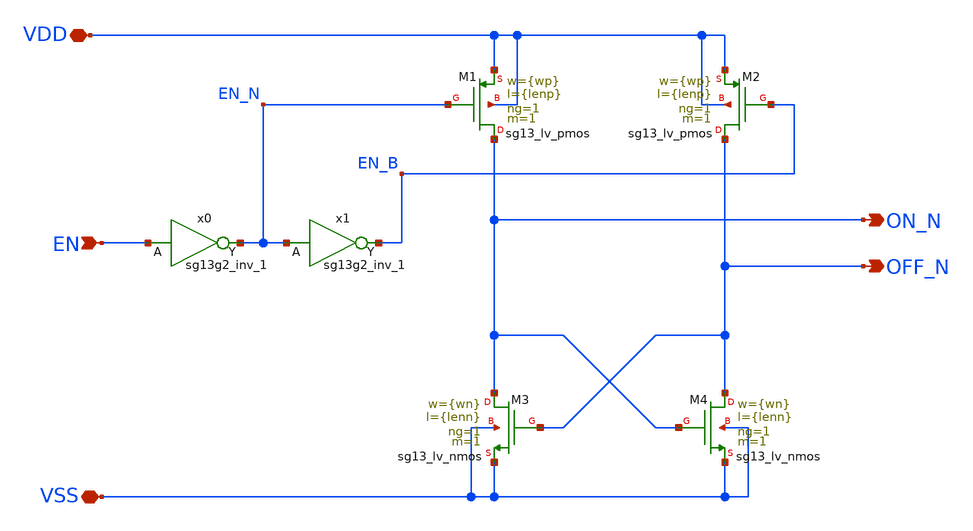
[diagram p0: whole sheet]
** sch_path: xschem/switch_logic_RS.sch
**.subckt switch_logic_RS VSS EN ON_N OFF_N VDD
*.iopin VSS
*.ipin EN
*.opin ON_N
*.opin OFF_N
*.iopin VDD
x0 EN_N EN VDD VSS sg13g2_inv_1
XM1 ON_N EN_N VDD VDD sg13_lv_pmos w={wp} l={lenp} ng=1 m=1 mm_ok=1
XM2 OFF_N EN_B VDD VDD sg13_lv_pmos w={wp} l={lenp} ng=1 m=1 mm_ok=1
XM3 ON_N OFF_N VSS VSS sg13_lv_nmos w={wn} l={lenn} ng=1 m=1 mm_ok=1
XM4 OFF_N ON_N VSS VSS sg13_lv_nmos w={wn} l={lenn} ng=1 m=1 mm_ok=1
x1 EN_B EN_N VDD VSS sg13g2_inv_1
**.ends

* expanding   symbol:  sg13g2_stdcells/sg13g2_inv_1.sym # of pins=2
** sym_path: sg13g2_stdcells/sg13g2_inv_1.sym
** sch_path: sg13g2_stdcells/sg13g2_inv_1.sch
.subckt sg13g2_inv_1 Y A VDD VSS
*.opin Y
*.ipin A
*.iopin VDD
*.iopin VSS
XM1 Y A VSS VSS sg13_lv_nmos w=740.00n l=130.00n ng=1 m=1 mm_ok=1
XM2 Y A VDD VDD sg13_lv_pmos w=1.12u l=130.00n ng=1 m=1 mm_ok=1
.ends

.end
